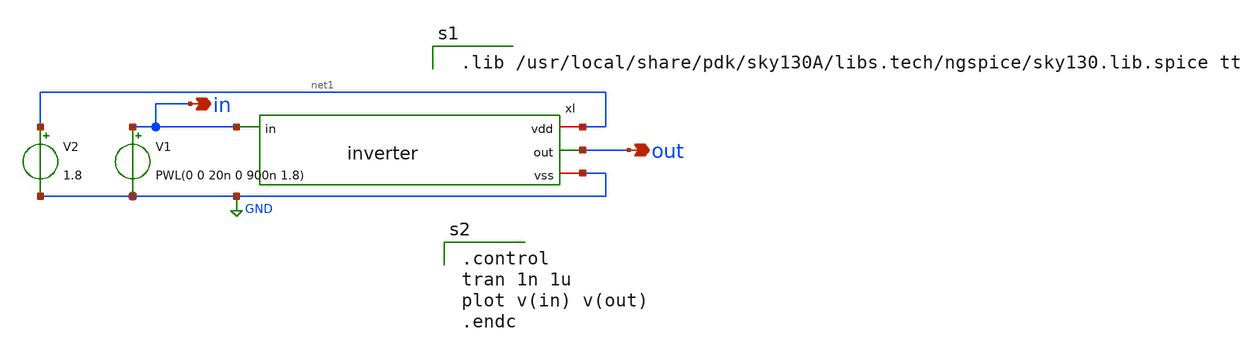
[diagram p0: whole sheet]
** sch_path: inverter/xschem/inverter_tb.sch
**.subckt inverter_tb out in
*.opin out
*.opin in
x1 net1 in out GND inverter
V1 in GND PWL(0 0 20n 0 900n 1.8)
V2 net1 GND 1.8
**** begin user architecture code

 .lib /usr/local/share/pdk/sky130A/libs.tech/ngspice/sky130.lib.spice tt


.control
tran 1n 1u
plot v(in) v(out)
.endc

**** end user architecture code
**.ends
.GLOBAL GND
.end
